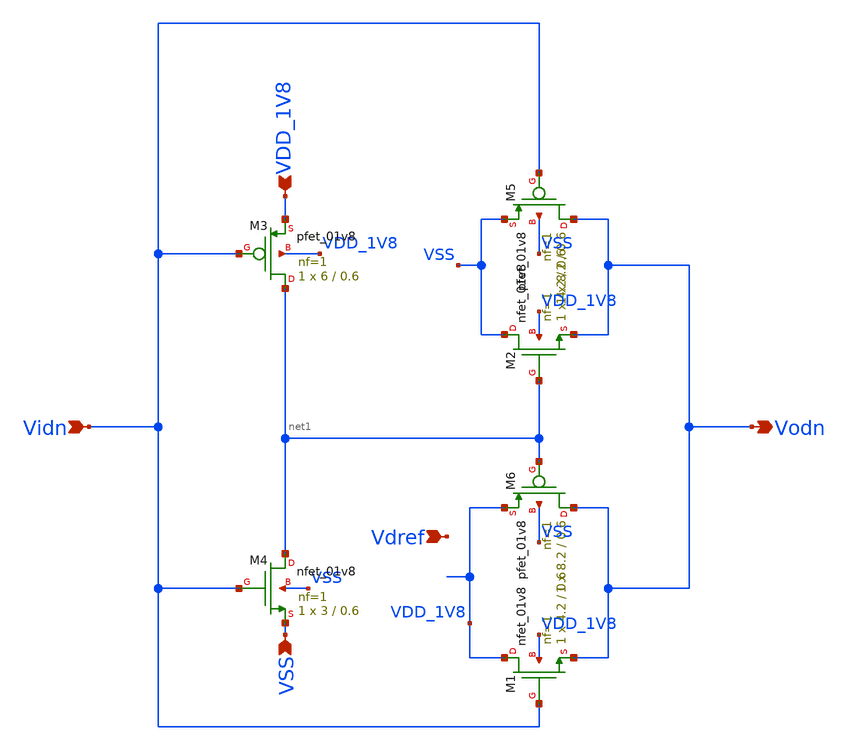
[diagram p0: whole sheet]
** sch_path: design/CNR_GR06_SKY130NM/dac_n.sch
**.subckt dac_n VDD_1V8 VSS Vidn Vodn Vdref
*.ipin VDD_1V8
*.ipin VSS
*.ipin Vidn
*.opin Vodn
*.ipin Vdref
XM3 net1 Vidn VDD_1V8 VDD_1V8 sky130_fd_pr__pfet_01v8 L=0.6 W=6 nf=1 ad='int((nf+1)/2) * W/nf * 0.29'
+ as='int((nf+2)/2) * W/nf * 0.29' pd='2*int((nf+1)/2) * (W/nf + 0.29)' ps='2*int((nf+2)/2) * (W/nf + 0.29)'
+ nrd='0.29 / W' nrs='0.29 / W' sa=0 sb=0 sd=0 mult=1 m=1
XM4 net1 Vidn VSS VSS sky130_fd_pr__nfet_01v8 L=0.6 W=3 nf=1 ad='int((nf+1)/2) * W/nf * 0.29' as='int((nf+2)/2) * W/nf * 0.29'
+ pd='2*int((nf+1)/2) * (W/nf + 0.29)' ps='2*int((nf+2)/2) * (W/nf + 0.29)' nrd='0.29 / W' nrs='0.29 / W'
+ sa=0 sb=0 sd=0 mult=1 m=1
XM1 VDD_1V8 Vidn Vodn VDD_1V8 sky130_fd_pr__nfet_01v8 L=0.6 W=4.2 nf=1 ad='int((nf+1)/2) * W/nf * 0.29'
+ as='int((nf+2)/2) * W/nf * 0.29' pd='2*int((nf+1)/2) * (W/nf + 0.29)' ps='2*int((nf+2)/2) * (W/nf + 0.29)'
+ nrd='0.29 / W' nrs='0.29 / W' sa=0 sb=0 sd=0 mult=1 m=1
XM2 VSS net1 Vodn VDD_1V8 sky130_fd_pr__nfet_01v8 L=0.6 W=4.2 nf=1 ad='int((nf+1)/2) * W/nf * 0.29' as='int((nf+2)/2) * W/nf * 0.29'
+ pd='2*int((nf+1)/2) * (W/nf + 0.29)' ps='2*int((nf+2)/2) * (W/nf + 0.29)' nrd='0.29 / W' nrs='0.29 / W'
+ sa=0 sb=0 sd=0 mult=1 m=1
XM5 Vodn Vidn VSS VSS sky130_fd_pr__pfet_01v8 L=0.6 W=8.2 nf=1 ad='int((nf+1)/2) * W/nf * 0.29' as='int((nf+2)/2) * W/nf * 0.29'
+ pd='2*int((nf+1)/2) * (W/nf + 0.29)' ps='2*int((nf+2)/2) * (W/nf + 0.29)' nrd='0.29 / W' nrs='0.29 / W'
+ sa=0 sb=0 sd=0 mult=1 m=1
XM6 Vodn net1 VDD_1V8 VSS sky130_fd_pr__pfet_01v8 L=0.6 W=8.2 nf=1 ad='int((nf+1)/2) * W/nf * 0.29' as='int((nf+2)/2) * W/nf * 0.29'
+ pd='2*int((nf+1)/2) * (W/nf + 0.29)' ps='2*int((nf+2)/2) * (W/nf + 0.29)' nrd='0.29 / W' nrs='0.29 / W'
+ sa=0 sb=0 sd=0 mult=1 m=1
**.ends
.end
